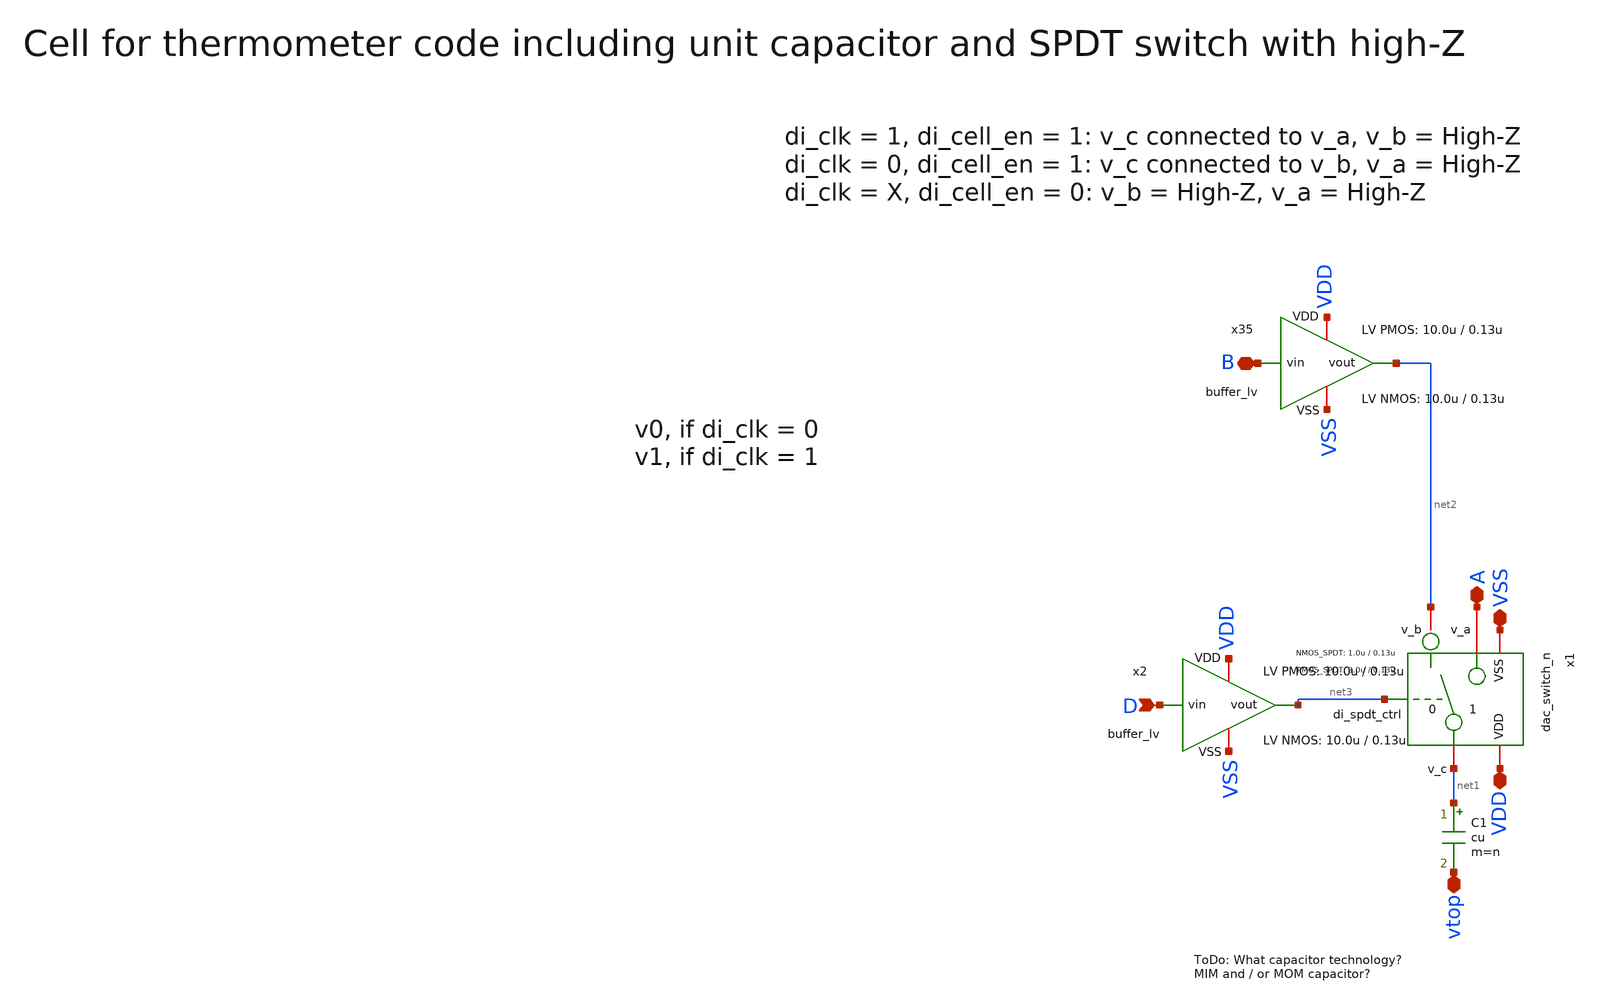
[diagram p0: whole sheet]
** sch_path: xschem/dac_icms_cell/unit_cell_n.sch
* IHP-GmbH/IHP-Open-PDK/ihp-sg13g2/libs.tech/xschem/sg13g2_stdcells/sg13g2_dlygate4sd2_1.sch:
* Copyright 2023 IHP PDK Authors
* Licensed under the Apache License, Version 2.0 (the "License");
**.subckt unit_cell_n VSS A VDD D B vtop
*.iopin VSS
*.iopin A
*.iopin VDD
*.ipin D
*.iopin B
*.iopin vtop
x1 VDD net3 VSS net1 net2 A dac_switch_n W_P_TG=3.0u L_P_TG=0.13u W_N_TG=1.0u L_N_TG=0.13u n={1}
C1 net1 vtop cu m=n
x35 VDD B net2 VSS buffer_lv W_P_INV=10.0u L_P_INV=0.13u W_N_INV=10.0u L_N_INV=0.13u
x2 VDD D net3 VSS buffer_lv W_P_INV=10.0u L_P_INV=0.13u W_N_INV=10.0u L_N_INV=0.13u
**.ends

* expanding   symbol:  dac_icms_cell/dac_switch_n.sym # of pins=6
** sym_path: xschem/dac_icms_cell/dac_switch_n.sym
** sch_path: xschem/dac_icms_cell/dac_switch_n.sch
.subckt dac_switch_n VDD di_spdt_ctrl VSS v_c v_b v_a  W_P_TG=3.0u L_P_TG=0.13u W_N_TG=1.0u
+ L_N_TG=0.13u n=1
*.iopin v_a
*.iopin v_c
*.iopin VDD
*.iopin VSS
*.ipin di_spdt_ctrl
*.iopin v_b
x1 VDD di_spdt_ctrl VSS v_c v_a di_spdt_ctrl_n transmission_gate_lv_wo_dummy W_P=W_P_TG L_P=L_P_TG
+ W_N=W_N_TG L_N=L_N_TG W_P_D=1.0u L_P_D=0.13u W_N_D=1.0u L_N_D=0.13u n=n
x8 VDD di_spdt_ctrl di_spdt_ctrl_n VSS inverter_lv W_P=W_P_TG L_P=L_P_TG W_N=W_N_TG L_N=L_N_TG n=n
XM1 net1 net2 VSS VSS sg13_lv_nmos w=0.5u l=0.2u ng=1 m=n mm_ok=1
XM3 net1 net2 VDD VDD sg13_lv_pmos w=1u l=0.2u ng=1 m=n mm_ok=1
x2 VDD net3 VSS net1 v_c net4 transmission_gate_lv_w_dummy W_P=W_P_TG L_P=L_P_TG W_N=W_N_TG
+ L_N=L_N_TG W_P_D=1.0u L_P_D=0.13u W_N_D=1.0u L_N_D=0.13u n=n
XM2 net2 v_b VSS VSS sg13_lv_nmos w=0.5u l=0.2u ng=1 m=n mm_ok=1
XM4 net2 v_b VDD VDD sg13_lv_pmos w=1u l=0.2u ng=1 m=n mm_ok=1
x40 net3 di_spdt_ctrl_n VDD VSS sg13g2_dlygate4sd2_1
x3 net4 di_spdt_ctrl VDD VSS sg13g2_dlygate4sd2_1
.ends


* expanding   symbol:  buffer/buffer_lv.sym # of pins=4
** sym_path: buffer/buffer_lv.sym
** sch_path: buffer/buffer_lv.sch
.subckt buffer_lv VDD vin vout VSS  W_P_INV=3.0u L_P_INV=0.13u W_N_INV=1.0u L_N_INV=0.13u
*.ipin vin
*.iopin VDD
*.iopin VSS
*.opin vout
x1 VDD vin net1 VSS inverter_lv W_P=W_P_INV L_P=L_P_INV W_N=W_N_INV L_N=L_N_INV n=1
x2 VDD net1 vout VSS inverter_lv W_P=W_P_INV L_P=L_P_INV W_N=W_N_INV L_N=L_N_INV n=1
.ends


* expanding   symbol:  transmission_gate/transmission_gate_lv_wo_dummy.sym # of pins=6
** sym_path: xschem/transmission_gate/transmission_gate_lv_wo_dummy.sym
** sch_path: xschem/transmission_gate/transmission_gate_lv_wo_dummy.sch
.subckt transmission_gate_lv_wo_dummy VDD di_tg_ctrl VSS v_b v_a di_tg_ctrl_n  W_P=2.0u L_P=0.13u
+ W_N=2.0u L_N=0.13u W_P_D=1.0u L_P_D=0.13u W_N_D=1.0u L_N_D=0.13u n=1
*.iopin v_a
*.iopin v_b
*.iopin VDD
*.iopin VSS
*.ipin di_tg_ctrl
*.ipin di_tg_ctrl_n
XM1 v_a di_tg_ctrl v_b VSS sg13_lv_nmos w=W_N l=L_N ng=1 m=n mm_ok=1
XM2 v_a di_tg_ctrl_n v_b VDD sg13_lv_pmos w=W_P l=L_P ng=1 m=n mm_ok=1
.ends


* expanding   symbol:  inverter/inverter_lv.sym # of pins=4
** sym_path: xschem/inverter/inverter_lv.sym
** sch_path: xschem/inverter/inverter_lv.sch
.subckt inverter_lv VDD vin vout VSS  W_P=3.0u L_P=0.13u W_N=1.0u L_N=0.13u n=1
*.ipin vin
*.iopin VDD
*.iopin VSS
*.opin vout
XM1 vout vin VDD VDD sg13_lv_pmos w=W_P l=L_P ng=1 m=n mm_ok=1
XM2 vout vin VSS VSS sg13_lv_nmos w=W_N l=L_N ng=1 m=n mm_ok=1
.ends


* expanding   symbol:  transmission_gate/transmission_gate_lv_w_dummy.sym # of pins=6
** sym_path: xschem/transmission_gate/transmission_gate_lv_w_dummy.sym
** sch_path: xschem/transmission_gate/transmission_gate_lv_w_dummy.sch
.subckt transmission_gate_lv_w_dummy VDD di_tg_ctrl VSS v_b v_a di_tg_ctrl_n  W_P=2.0u L_P=0.13u
+ W_N=2.0u L_N=0.13u W_P_D=1.0u L_P_D=0.13u W_N_D=1.0u L_N_D=0.13u n=1
*.iopin v_a
*.iopin v_b
*.iopin VDD
*.iopin VSS
*.ipin di_tg_ctrl
*.ipin di_tg_ctrl_n
XM1 v_a di_tg_ctrl v_b VSS sg13_lv_nmos w=W_N l=L_N ng=1 m=n mm_ok=1
XM2 v_a di_tg_ctrl_n v_b VDD sg13_lv_pmos w=W_P l=L_P ng=1 m=n mm_ok=1
XMdummy2 v_b di_tg_ctrl v_b VDD sg13_lv_pmos w=W_P_D l=L_P_D ng=1 m=n mm_ok=1
XMdummy1 v_b di_tg_ctrl_n v_b VSS sg13_lv_nmos w=W_N_D l=L_N_D ng=1 m=n mm_ok=1
.ends


* expanding   symbol:  sg13g2_stdcells/sg13g2_dlygate4sd2_1.sym # of pins=2
** sym_path: sg13g2_stdcells/sg13g2_dlygate4sd2_1.sym
** sch_path: sg13g2_stdcells/sg13g2_dlygate4sd2_1.sch
.subckt sg13g2_dlygate4sd2_1 X A VDD VSS
*.ipin A
*.opin X
*.iopin VDD
*.iopin VSS
XM1 net2 A VSS VSS sg13_lv_nmos w=420.00n l=130.00n ng=1 m=1 mm_ok=1
XM2 net1 net2 VSS VSS sg13_lv_nmos w=420.00n l=180.00n ng=1 m=1 mm_ok=1
XM3 net3 net1 VSS VSS sg13_lv_nmos w=420.00n l=180.00n ng=1 m=1 mm_ok=1
XM4 X net3 VSS VSS sg13_lv_nmos w=740.00n l=130.00n ng=1 m=1 mm_ok=1
XM5 net2 A VDD VDD sg13_lv_pmos w=420.00n l=130.00n ng=1 m=1 mm_ok=1
XM6 net1 net2 VDD VDD sg13_lv_pmos w=1.000u l=250.00n ng=1 m=1 mm_ok=1
XM7 net3 net1 VDD VDD sg13_lv_pmos w=1.000u l=250.00n ng=1 m=1 mm_ok=1
XM8 X net3 VDD VDD sg13_lv_pmos w=1.12u l=130.00n ng=1 m=1 mm_ok=1
.ends

.end
